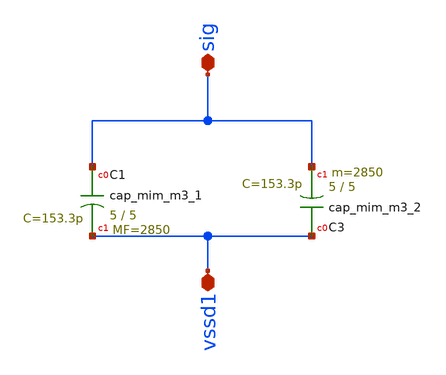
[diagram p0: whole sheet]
** sch_path: xschem/mimcap_stacked_57x50.sch
**.subckt mimcap_stacked_57x50 vssd1 sig
*.iopin vssd1
*.iopin sig
XC1 sig vssd1 sky130_fd_pr__cap_mim_m3_1 W=5 L=5 MF=2850 m=2850
XC3 vssd1 sig sky130_fd_pr__cap_mim_m3_2 W=5 L=5 MF=2850 m=2850
**.ends
.end
